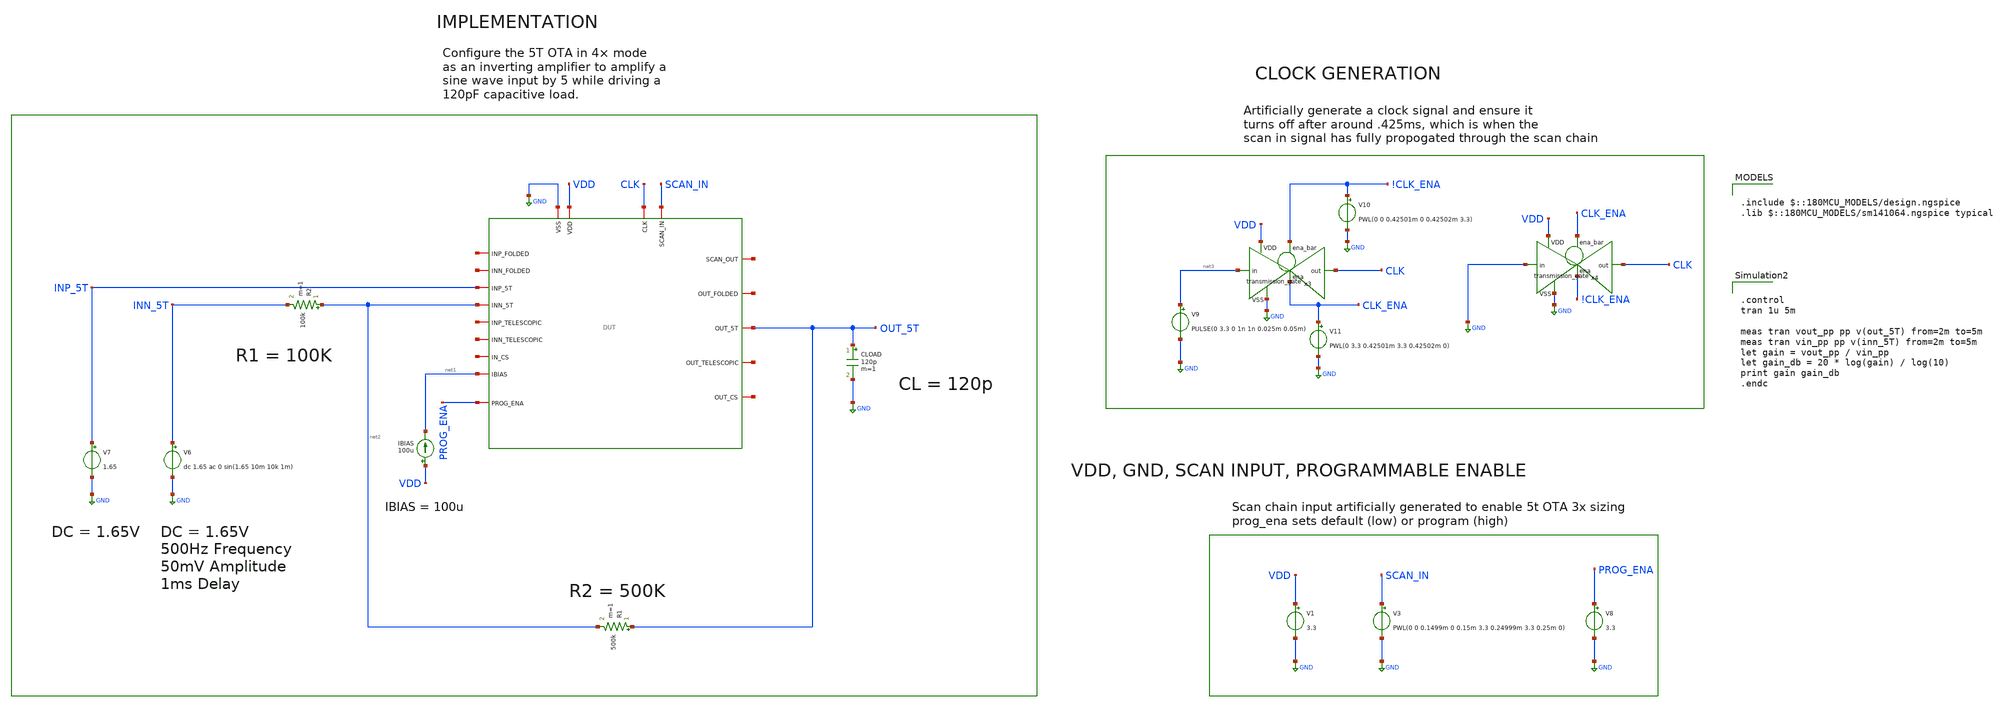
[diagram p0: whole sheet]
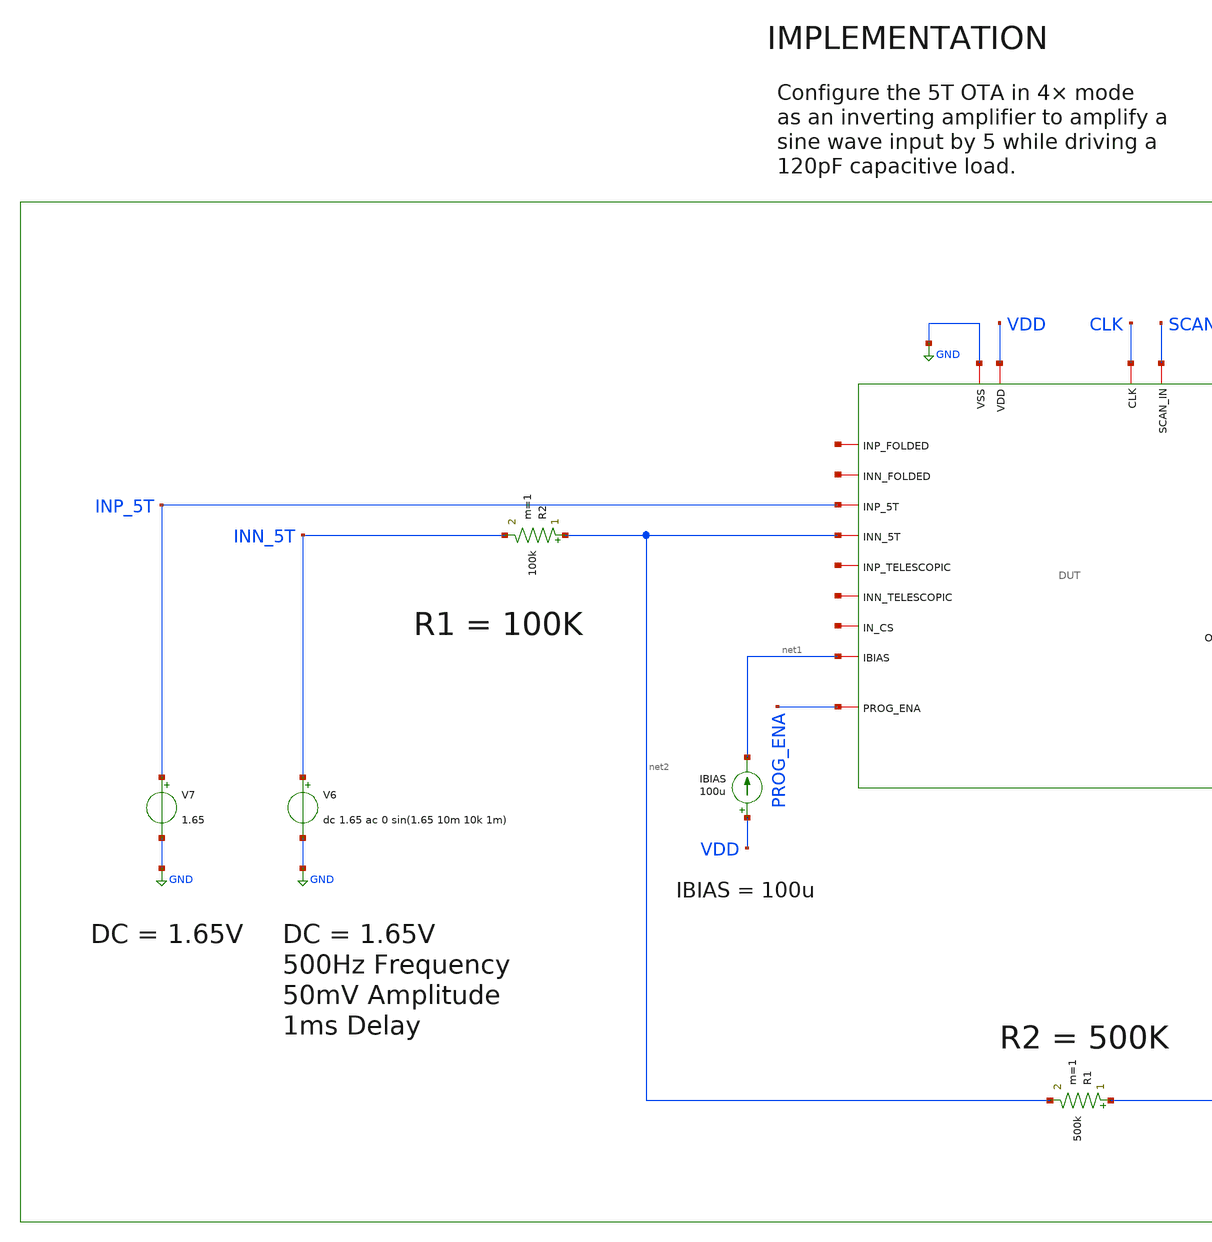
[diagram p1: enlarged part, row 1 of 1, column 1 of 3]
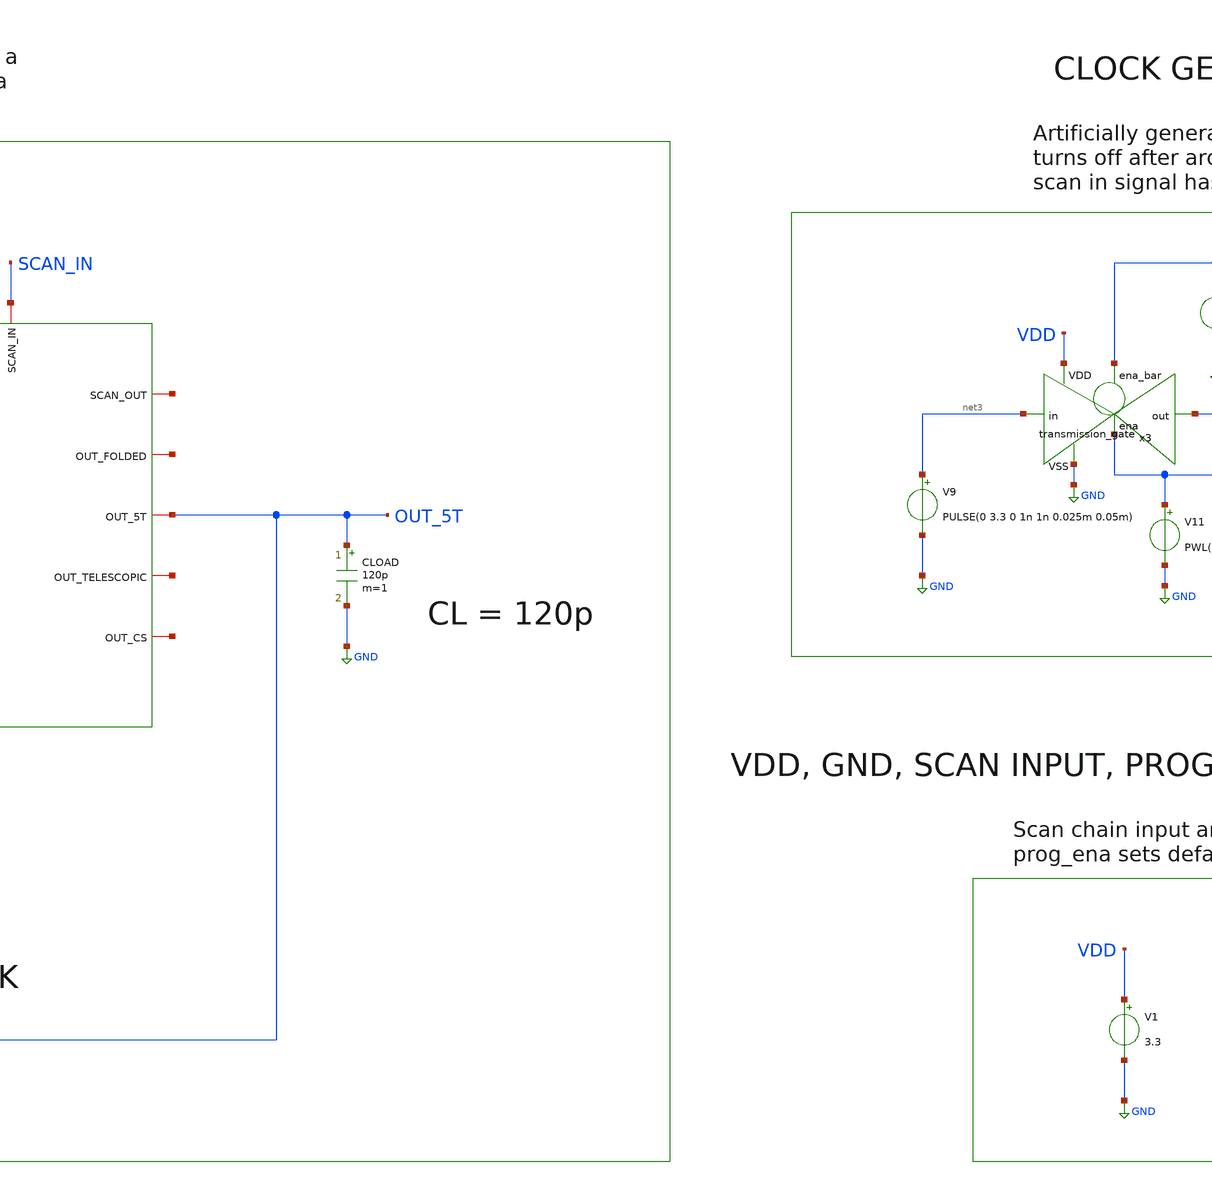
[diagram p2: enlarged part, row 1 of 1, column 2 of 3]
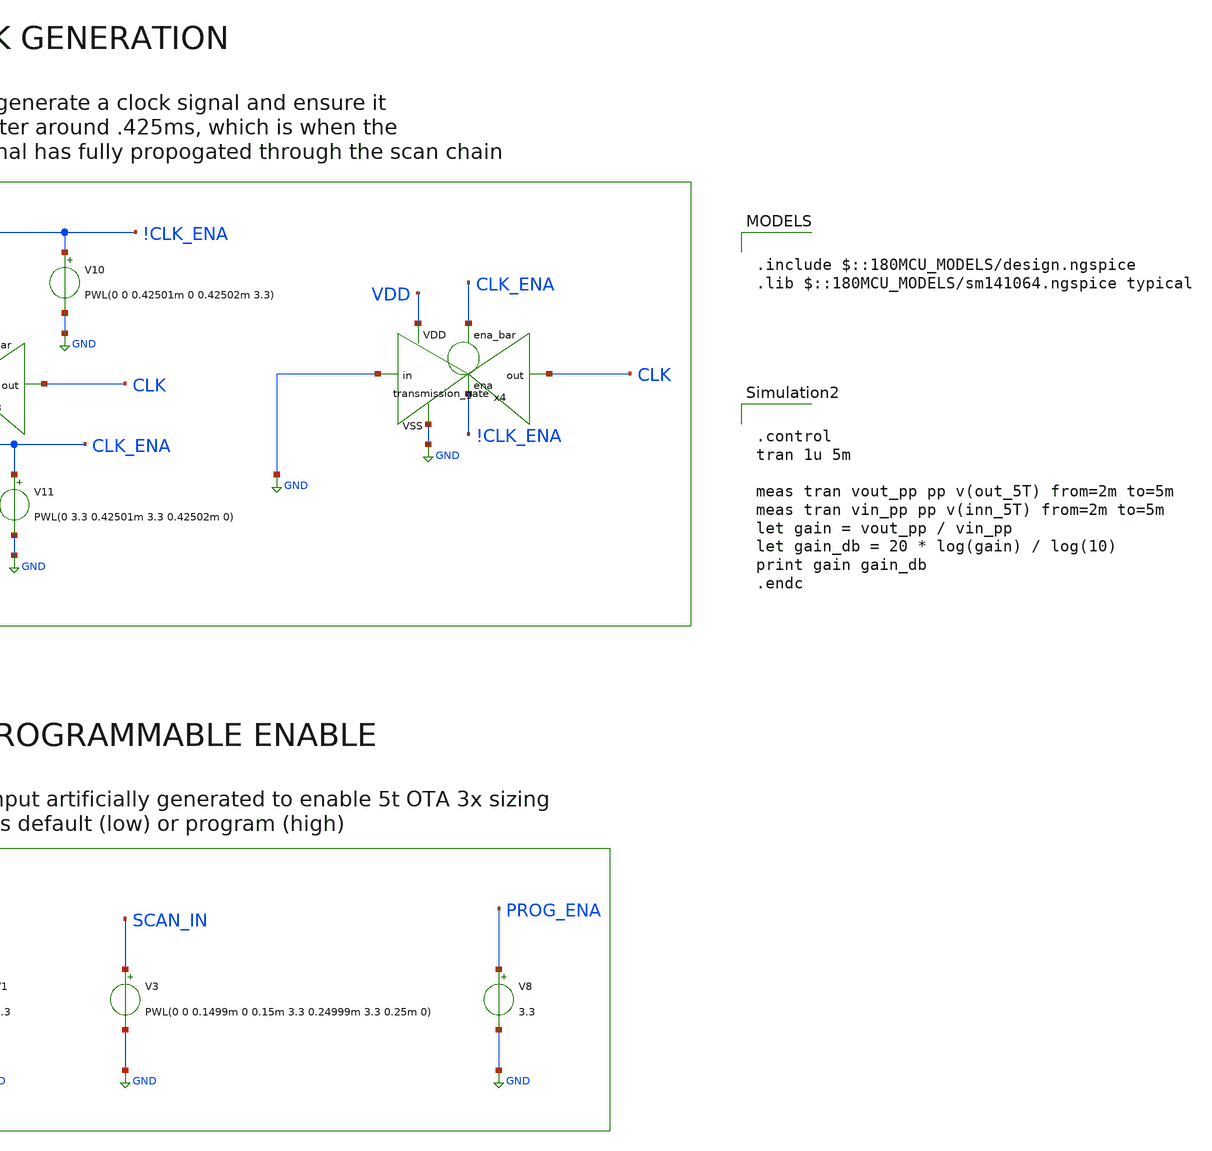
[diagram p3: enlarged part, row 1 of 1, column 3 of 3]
** sch_path: designs/libs/verification/ota_5t/4x_sizing/5t_4x_bandwidth_tb.sch
**.subckt 5t_4x_bandwidth_tb
V3 SCAN_IN GND PWL(0 0 0.1499m 0 0.15m 3.3 0.24999m 3.3 0.25m 0)
V1 VDD GND 3.3
IBIAS VDD net1 100u
V7 INP_5T GND 1.65
CLOAD OUT_5T GND 120p m=1
R2 net2 INN_5T 100k m=1
V6 INN_5T GND dc 1.65 ac 0 sin(1.65 10m 10k 1m)
R1 OUT_5T net2 500k m=1
x1 CLK net4 SCAN_IN GND VDD net5 net6 OUT_5T net1 net7 INP_5T net2 net8 net9 net10 net11 net12
+ PROG_ENA DUT
V8 PROG_ENA GND 3.3
V9 net3 GND PULSE(0 3.3 0 1n 1n 0.025m 0.05m)
x3 !CLK_ENA VDD CLK net3 GND CLK_ENA transmission_gate
V10 !CLK_ENA GND PWL(0 0 0.42501m 0 0.42502m 3.3)
V11 CLK_ENA GND PWL(0 3.3 0.42501m 3.3 0.42502m 0)
x4 CLK_ENA VDD CLK GND GND !CLK_ENA transmission_gate
**** begin user architecture code

.include $::180MCU_MODELS/design.ngspice
.lib $::180MCU_MODELS/sm141064.ngspice typical



.control
tran 1u 5m

meas tran vout_pp pp v(out_5T) from=2m to=5m
meas tran vin_pp pp v(inn_5T) from=2m to=5m
let gain = vout_pp / vin_pp
let gain_db = 20 * log(gain) / log(10)
print gain gain_db
.endc


**** end user architecture code
**.ends
.GLOBAL GND
.end
